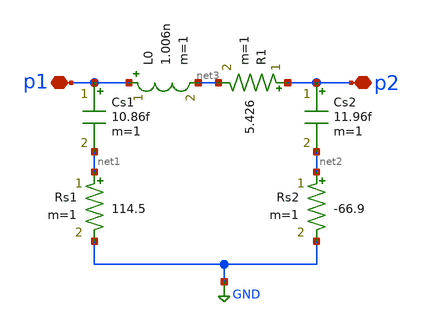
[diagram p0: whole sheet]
** sch_path: ask_modulator/xschem/l0.sch
**.subckt l0 p2 p1
*.iopin p2
*.iopin p1
L0 p1 net3 1.006n m=1
Cs1 p1 net1 10.86f m=1
Cs2 p2 net2 11.96f m=1
Rs1 net1 GND 114.5 m=1
Rs2 net2 GND -66.9 m=1
R1 p2 net3 5.426 m=1
**.ends
.GLOBAL GND
.end
